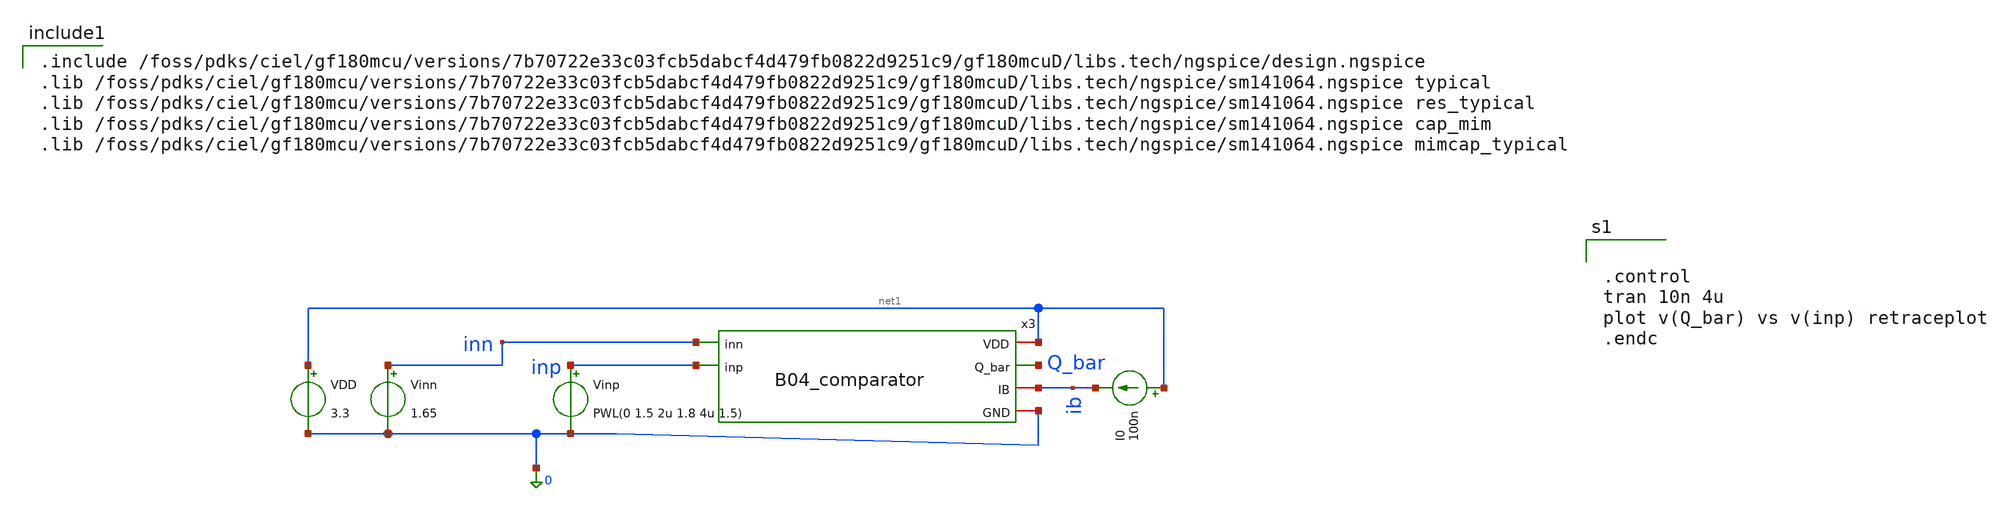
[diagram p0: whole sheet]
** sch_path: analog/B04_tb_comparator.sch
**.subckt B04_tb_comparator
Vinn inn 0 1.65
VDD net1 0 3.3
x3 net1 Q_bar inn inp ib 0 B04_comparator
Vinp inp 0 PWL(0 1.5 2u 1.8 4u 1.5)
I0 net1 ib 100n
**** begin user architecture code

.include /foss/pdks/ciel/gf180mcu/versions/7b70722e33c03fcb5dabcf4d479fb0822d9251c9/gf180mcuD/libs.tech/ngspice/design.ngspice
.lib /foss/pdks/ciel/gf180mcu/versions/7b70722e33c03fcb5dabcf4d479fb0822d9251c9/gf180mcuD/libs.tech/ngspice/sm141064.ngspice typical
.lib /foss/pdks/ciel/gf180mcu/versions/7b70722e33c03fcb5dabcf4d479fb0822d9251c9/gf180mcuD/libs.tech/ngspice/sm141064.ngspice res_typical
.lib /foss/pdks/ciel/gf180mcu/versions/7b70722e33c03fcb5dabcf4d479fb0822d9251c9/gf180mcuD/libs.tech/ngspice/sm141064.ngspice cap_mim
.lib /foss/pdks/ciel/gf180mcu/versions/7b70722e33c03fcb5dabcf4d479fb0822d9251c9/gf180mcuD/libs.tech/ngspice/sm141064.ngspice mimcap_typical



.control
tran 10n 4u
plot v(Q_bar) vs v(inp) retraceplot
.endc


**** end user architecture code
**.ends

* expanding   symbol:
*+  AURA-Event-Driven-Mixed-Signal-ASIC-for-Acoustic-Pattern-Detection/analog/B04_comparator.sym # of pins=6
** sym_path: analog/B04_comparator.sym
** sch_path: analog/B04_comparator.sch
.subckt B04_comparator VDD Q_bar inn inp IB GND
*.iopin VDD
*.iopin GND
*.ipin inn
*.ipin inp
*.iopin IB
*.opin Q_bar
XM1 net2 IB GND GND nfet_03v3 L=0.56u W=1u nf=1 ad='int((nf+1)/2) * W/nf * 0.18u' as='int((nf+2)/2) * W/nf * 0.18u'
+ pd='2*int((nf+1)/2) * (W/nf + 0.18u)' ps='2*int((nf+2)/2) * (W/nf + 0.18u)' nrd='0.18u / W' nrs='0.18u / W'
+ sa=0 sb=0 sd=0 m=1
XM2 IB IB GND GND nfet_03v3 L=0.56u W=1u nf=1 ad='int((nf+1)/2) * W/nf * 0.18u' as='int((nf+2)/2) * W/nf * 0.18u'
+ pd='2*int((nf+1)/2) * (W/nf + 0.18u)' ps='2*int((nf+2)/2) * (W/nf + 0.18u)' nrd='0.18u / W' nrs='0.18u / W'
+ sa=0 sb=0 sd=0 m=1
XM3 net1 net1 GND GND nfet_03v3 L=0.56u W=1u nf=1 ad='int((nf+1)/2) * W/nf * 0.18u' as='int((nf+2)/2) * W/nf * 0.18u'
+ pd='2*int((nf+1)/2) * (W/nf + 0.18u)' ps='2*int((nf+2)/2) * (W/nf + 0.18u)' nrd='0.18u / W' nrs='0.18u / W'
+ sa=0 sb=0 sd=0 m=1
Xqqq net3 inn net2 GND nfet_03v3 L=0.28u W=2u nf=1 ad='int((nf+1)/2) * W/nf * 0.18u' as='int((nf+2)/2) * W/nf * 0.18u'
+ pd='2*int((nf+1)/2) * (W/nf + 0.18u)' ps='2*int((nf+2)/2) * (W/nf + 0.18u)' nrd='0.18u / W' nrs='0.18u / W'
+ sa=0 sb=0 sd=0 m=1
Xqqq1 net4 inp net2 GND nfet_03v3 L=0.28u W=2u nf=1 ad='int((nf+1)/2) * W/nf * 0.18u' as='int((nf+2)/2) * W/nf * 0.18u'
+ pd='2*int((nf+1)/2) * (W/nf + 0.18u)' ps='2*int((nf+2)/2) * (W/nf + 0.18u)' nrd='0.18u / W' nrs='0.18u / W'
+ sa=0 sb=0 sd=0 m=1
XM6 Q_bar net1 GND GND nfet_03v3 L=0.56u W=1u nf=1 ad='int((nf+1)/2) * W/nf * 0.18u' as='int((nf+2)/2) * W/nf * 0.18u'
+ pd='2*int((nf+1)/2) * (W/nf + 0.18u)' ps='2*int((nf+2)/2) * (W/nf + 0.18u)' nrd='0.18u / W' nrs='0.18u / W'
+ sa=0 sb=0 sd=0 m=1
Xq net3 net3 VDD VDD pfet_03v3 L=0.28u W=1.5u nf=1 ad='int((nf+1)/2) * W/nf * 0.18u' as='int((nf+2)/2) * W/nf * 0.18u'
+ pd='2*int((nf+1)/2) * (W/nf + 0.18u)' ps='2*int((nf+2)/2) * (W/nf + 0.18u)' nrd='0.18u / W' nrs='0.18u / W'
+ sa=0 sb=0 sd=0 m=1
Xq1 net1 net3 VDD VDD pfet_03v3 L=0.28u W=1.5u nf=1 ad='int((nf+1)/2) * W/nf * 0.18u' as='int((nf+2)/2) * W/nf * 0.18u'
+ pd='2*int((nf+1)/2) * (W/nf + 0.18u)' ps='2*int((nf+2)/2) * (W/nf + 0.18u)' nrd='0.18u / W' nrs='0.18u / W'
+ sa=0 sb=0 sd=0 m=1
Xq4 net3 net4 VDD VDD pfet_03v3 L=0.28u W=3.5u nf=1 ad='int((nf+1)/2) * W/nf * 0.18u' as='int((nf+2)/2) * W/nf * 0.18u'
+ pd='2*int((nf+1)/2) * (W/nf + 0.18u)' ps='2*int((nf+2)/2) * (W/nf + 0.18u)' nrd='0.18u / W' nrs='0.18u / W'
+ sa=0 sb=0 sd=0 m=1
Xq5 net4 net3 VDD VDD pfet_03v3 L=0.28u W=3.5u nf=1 ad='int((nf+1)/2) * W/nf * 0.18u' as='int((nf+2)/2) * W/nf * 0.18u'
+ pd='2*int((nf+1)/2) * (W/nf + 0.18u)' ps='2*int((nf+2)/2) * (W/nf + 0.18u)' nrd='0.18u / W' nrs='0.18u / W'
+ sa=0 sb=0 sd=0 m=1
Xq2 net4 net4 VDD VDD pfet_03v3 L=0.28u W=1.5u nf=1 ad='int((nf+1)/2) * W/nf * 0.18u' as='int((nf+2)/2) * W/nf * 0.18u'
+ pd='2*int((nf+1)/2) * (W/nf + 0.18u)' ps='2*int((nf+2)/2) * (W/nf + 0.18u)' nrd='0.18u / W' nrs='0.18u / W'
+ sa=0 sb=0 sd=0 m=1
Xq3 Q_bar net4 VDD VDD pfet_03v3 L=0.28u W=1.5u nf=1 ad='int((nf+1)/2) * W/nf * 0.18u' as='int((nf+2)/2) * W/nf * 0.18u'
+ pd='2*int((nf+1)/2) * (W/nf + 0.18u)' ps='2*int((nf+2)/2) * (W/nf + 0.18u)' nrd='0.18u / W' nrs='0.18u / W'
+ sa=0 sb=0 sd=0 m=1
.ends

.end
